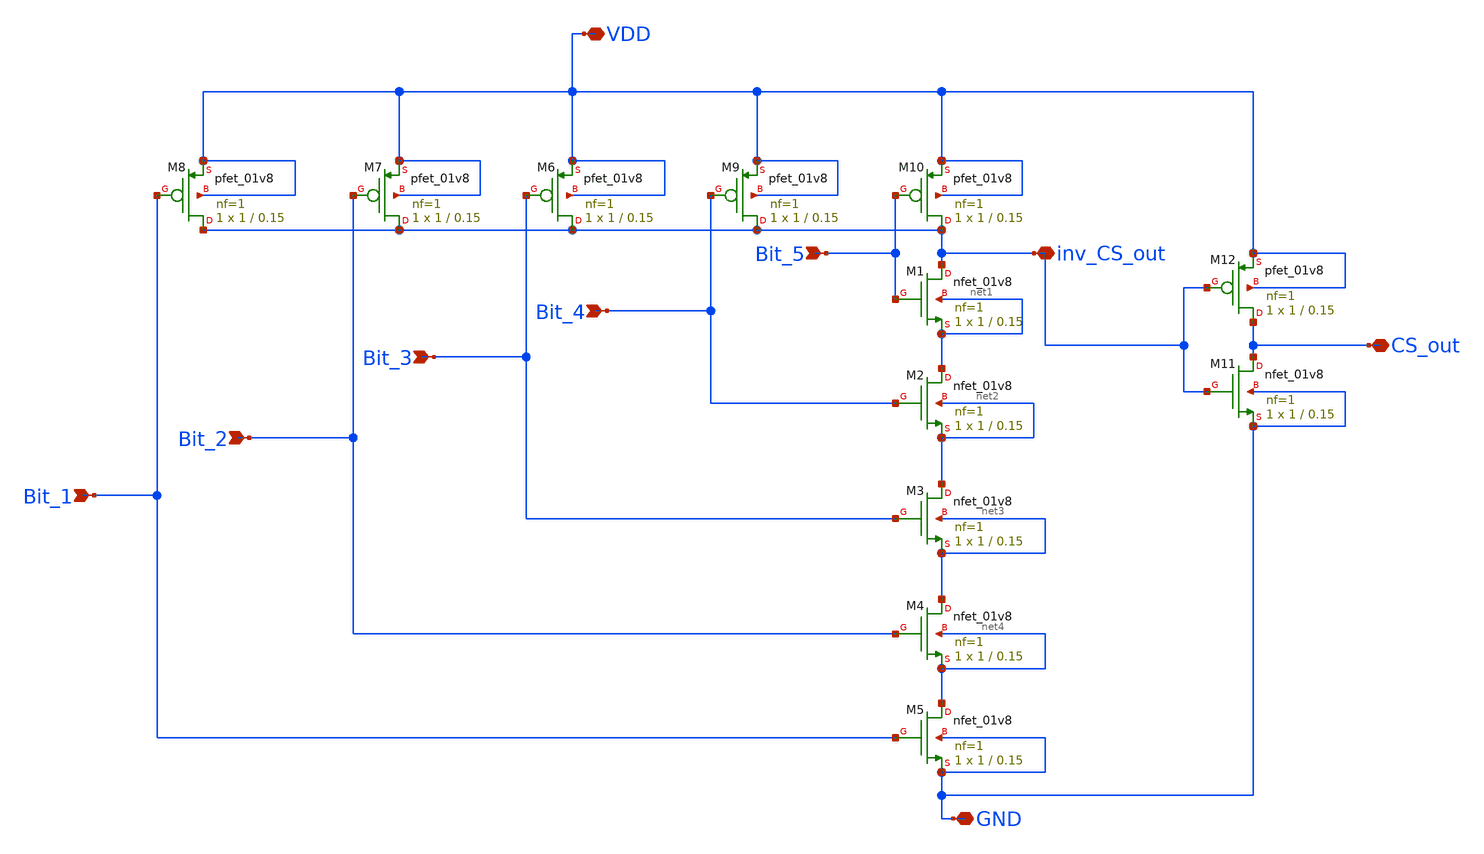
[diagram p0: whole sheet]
** sch_path: ProjectDesigns/5BitAND/5bit_AND.sch
**.subckt 5bit_AND Bit_1 Bit_3 Bit_2 Bit_4 Bit_5 inv_CS_out CS_out VDD GND
*.ipin Bit_1
*.ipin Bit_3
*.ipin Bit_2
*.ipin Bit_4
*.ipin Bit_5
*.iopin inv_CS_out
*.iopin CS_out
*.iopin VDD
*.iopin GND
XM1 inv_CS_out Bit_5 net1 net1 sky130_fd_pr__nfet_01v8 L=0.15 W=1 nf=1 ad='int((nf+1)/2) * W/nf * 0.29'
+ as='int((nf+2)/2) * W/nf * 0.29' pd='2*int((nf+1)/2) * (W/nf + 0.29)' ps='2*int((nf+2)/2) * (W/nf + 0.29)'
+ nrd='0.29 / W' nrs='0.29 / W' sa=0 sb=0 sd=0 mult=1 m=1
XM2 net1 Bit_4 net2 net2 sky130_fd_pr__nfet_01v8 L=0.15 W=1 nf=1 ad='int((nf+1)/2) * W/nf * 0.29' as='int((nf+2)/2) * W/nf * 0.29'
+ pd='2*int((nf+1)/2) * (W/nf + 0.29)' ps='2*int((nf+2)/2) * (W/nf + 0.29)' nrd='0.29 / W' nrs='0.29 / W'
+ sa=0 sb=0 sd=0 mult=1 m=1
XM3 net2 Bit_3 net3 net3 sky130_fd_pr__nfet_01v8 L=0.15 W=1 nf=1 ad='int((nf+1)/2) * W/nf * 0.29' as='int((nf+2)/2) * W/nf * 0.29'
+ pd='2*int((nf+1)/2) * (W/nf + 0.29)' ps='2*int((nf+2)/2) * (W/nf + 0.29)' nrd='0.29 / W' nrs='0.29 / W'
+ sa=0 sb=0 sd=0 mult=1 m=1
XM4 net3 Bit_2 net4 net4 sky130_fd_pr__nfet_01v8 L=0.15 W=1 nf=1 ad='int((nf+1)/2) * W/nf * 0.29' as='int((nf+2)/2) * W/nf * 0.29'
+ pd='2*int((nf+1)/2) * (W/nf + 0.29)' ps='2*int((nf+2)/2) * (W/nf + 0.29)' nrd='0.29 / W' nrs='0.29 / W'
+ sa=0 sb=0 sd=0 mult=1 m=1
XM5 net4 Bit_1 GND GND sky130_fd_pr__nfet_01v8 L=0.15 W=1 nf=1 ad='int((nf+1)/2) * W/nf * 0.29' as='int((nf+2)/2) * W/nf * 0.29'
+ pd='2*int((nf+1)/2) * (W/nf + 0.29)' ps='2*int((nf+2)/2) * (W/nf + 0.29)' nrd='0.29 / W' nrs='0.29 / W'
+ sa=0 sb=0 sd=0 mult=1 m=1
XM6 inv_CS_out Bit_3 VDD VDD sky130_fd_pr__pfet_01v8 L=0.15 W=1 nf=1 ad='int((nf+1)/2) * W/nf * 0.29'
+ as='int((nf+2)/2) * W/nf * 0.29' pd='2*int((nf+1)/2) * (W/nf + 0.29)' ps='2*int((nf+2)/2) * (W/nf + 0.29)'
+ nrd='0.29 / W' nrs='0.29 / W' sa=0 sb=0 sd=0 mult=1 m=1
XM7 inv_CS_out Bit_2 VDD VDD sky130_fd_pr__pfet_01v8 L=0.15 W=1 nf=1 ad='int((nf+1)/2) * W/nf * 0.29'
+ as='int((nf+2)/2) * W/nf * 0.29' pd='2*int((nf+1)/2) * (W/nf + 0.29)' ps='2*int((nf+2)/2) * (W/nf + 0.29)'
+ nrd='0.29 / W' nrs='0.29 / W' sa=0 sb=0 sd=0 mult=1 m=1
XM8 inv_CS_out Bit_1 VDD VDD sky130_fd_pr__pfet_01v8 L=0.15 W=1 nf=1 ad='int((nf+1)/2) * W/nf * 0.29'
+ as='int((nf+2)/2) * W/nf * 0.29' pd='2*int((nf+1)/2) * (W/nf + 0.29)' ps='2*int((nf+2)/2) * (W/nf + 0.29)'
+ nrd='0.29 / W' nrs='0.29 / W' sa=0 sb=0 sd=0 mult=1 m=1
XM9 inv_CS_out Bit_4 VDD VDD sky130_fd_pr__pfet_01v8 L=0.15 W=1 nf=1 ad='int((nf+1)/2) * W/nf * 0.29'
+ as='int((nf+2)/2) * W/nf * 0.29' pd='2*int((nf+1)/2) * (W/nf + 0.29)' ps='2*int((nf+2)/2) * (W/nf + 0.29)'
+ nrd='0.29 / W' nrs='0.29 / W' sa=0 sb=0 sd=0 mult=1 m=1
XM10 inv_CS_out Bit_5 VDD VDD sky130_fd_pr__pfet_01v8 L=0.15 W=1 nf=1 ad='int((nf+1)/2) * W/nf * 0.29'
+ as='int((nf+2)/2) * W/nf * 0.29' pd='2*int((nf+1)/2) * (W/nf + 0.29)' ps='2*int((nf+2)/2) * (W/nf + 0.29)'
+ nrd='0.29 / W' nrs='0.29 / W' sa=0 sb=0 sd=0 mult=1 m=1
XM11 CS_out inv_CS_out GND GND sky130_fd_pr__nfet_01v8 L=0.15 W=1 nf=1 ad='int((nf+1)/2) * W/nf * 0.29'
+ as='int((nf+2)/2) * W/nf * 0.29' pd='2*int((nf+1)/2) * (W/nf + 0.29)' ps='2*int((nf+2)/2) * (W/nf + 0.29)'
+ nrd='0.29 / W' nrs='0.29 / W' sa=0 sb=0 sd=0 mult=1 m=1
XM12 CS_out inv_CS_out VDD VDD sky130_fd_pr__pfet_01v8 L=0.15 W=1 nf=1 ad='int((nf+1)/2) * W/nf * 0.29'
+ as='int((nf+2)/2) * W/nf * 0.29' pd='2*int((nf+1)/2) * (W/nf + 0.29)' ps='2*int((nf+2)/2) * (W/nf + 0.29)'
+ nrd='0.29 / W' nrs='0.29 / W' sa=0 sb=0 sd=0 mult=1 m=1
**.ends
.end
